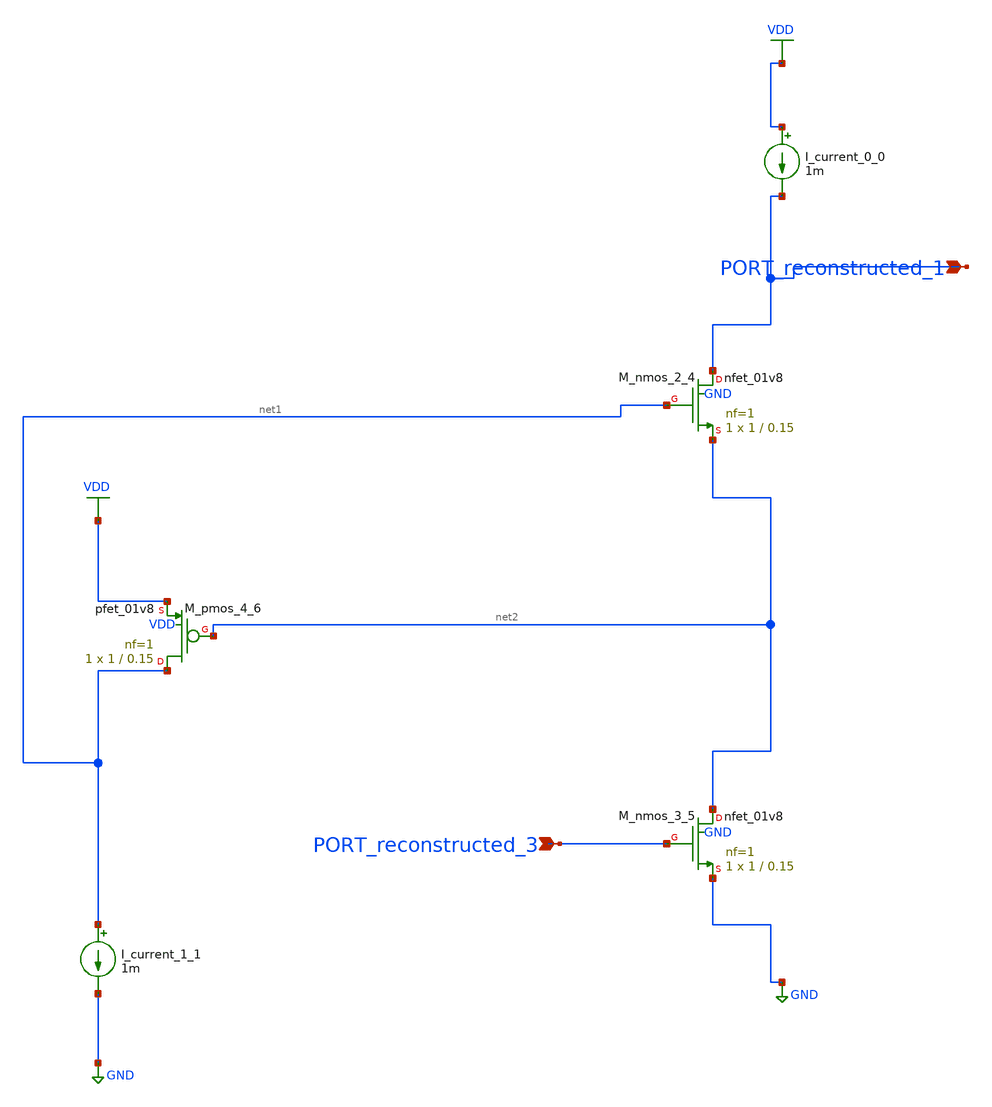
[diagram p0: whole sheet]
** sch_path: schematics/AMSNet/652.sch
**.subckt 652 PORT_reconstructed_3 PORT_reconstructed_1
*.ipin PORT_reconstructed_3
*.ipin PORT_reconstructed_1
I_current_0_0 VDD PORT_reconstructed_1 1m
I_current_1_1 net1 GND 1m
XM_nmos_2_4 PORT_reconstructed_1 net1 net2 GND sky130_fd_pr__nfet_01v8 L=0.15 W=1 nf=1 ad='int((1 + 1)/2) * 1 / 1 * 0.29'
+ as='int((1 + 2)/2) * 1 / 1 * 0.29' pd='2*int((1 + 1)/2) * (1 / 1 + 0.29)' ps='2*int((1 + 2)/2) * (1 / 1 + 0.29)'
+ nrd='0.29 / 1 ' nrs='0.29 / 1 ' sa=0 sb=0 sd=0 mult=1 m=1
XM_nmos_3_5 net2 PORT_reconstructed_3 GND GND sky130_fd_pr__nfet_01v8 L=0.15 W=1 nf=1 ad='int((1 + 1)/2) * 1 / 1 * 0.29'
+ as='int((1 + 2)/2) * 1 / 1 * 0.29' pd='2*int((1 + 1)/2) * (1 / 1 + 0.29)' ps='2*int((1 + 2)/2) * (1 / 1 + 0.29)'
+ nrd='0.29 / 1 ' nrs='0.29 / 1 ' sa=0 sb=0 sd=0 mult=1 m=1
XM_pmos_4_6 net1 net2 VDD VDD sky130_fd_pr__pfet_01v8 L=0.15 W=1 nf=1 ad='int((1 + 1)/2) * 1 / 1 * 0.29'
+ as='int((1 + 2)/2) * 1 / 1 * 0.29' pd='2*int((1 + 1)/2) * (1 / 1 + 0.29)' ps='2*int((1 + 2)/2) * (1 / 1 + 0.29)'
+ nrd='0.29 / 1 ' nrs='0.29 / 1 ' sa=0 sb=0 sd=0 mult=1 m=1
**.ends
.GLOBAL GND
.GLOBAL VDD
.end
